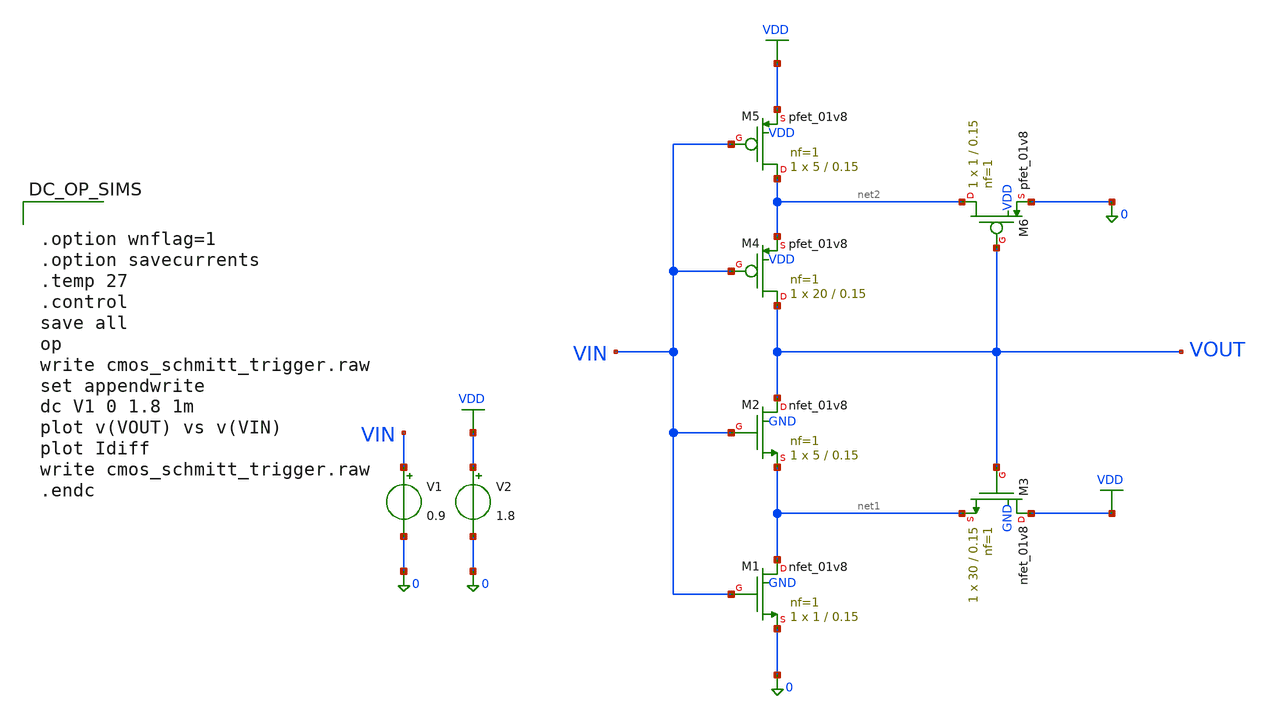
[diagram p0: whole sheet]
** sch_path: POR/cmos_sachmitt_trigger.sch
**.subckt cmos_sachmitt_trigger
XM1 net1 VIN 0 GND sky130_fd_pr__nfet_01v8 L=0.15 W=1 nf=1 ad='int((1 + 1)/2) * 1 / 1 * 0.29' as='int((1 + 2)/2) * 1 / 1 * 0.29'
+ pd='2*int((1 + 1)/2) * (1 / 1 + 0.29)' ps='2*int((1 + 2)/2) * (1 / 1 + 0.29)' nrd='0.29 / 1 ' nrs='0.29 / 1 '
+ sa=0 sb=0 sd=0 mult=1 m=1
XM2 VOUT VIN net1 GND sky130_fd_pr__nfet_01v8 L=0.15 W=5 nf=1 ad='int((1 + 1)/2) * 5 / 1 * 0.29' as='int((1 + 2)/2) * 5 / 1 * 0.29'
+ pd='2*int((1 + 1)/2) * (5 / 1 + 0.29)' ps='2*int((1 + 2)/2) * (5 / 1 + 0.29)' nrd='0.29 / 5 ' nrs='0.29 / 5 '
+ sa=0 sb=0 sd=0 mult=1 m=1
XM3 VDD VOUT net1 GND sky130_fd_pr__nfet_01v8 L=0.15 W=30 nf=1 ad='int((1 + 1)/2) * 30 / 1 * 0.29' as='int((1 + 2)/2) * 30 / 1 * 0.29'
+ pd='2*int((1 + 1)/2) * (30 / 1 + 0.29)' ps='2*int((1 + 2)/2) * (30 / 1 + 0.29)' nrd='0.29 / 30 ' nrs='0.29 / 30 '
+ sa=0 sb=0 sd=0 mult=1 m=1
XM4 VOUT VIN net2 VDD sky130_fd_pr__pfet_01v8 L=0.15 W=20 nf=1 ad='int((1 + 1)/2) * 20 / 1 * 0.29' as='int((1 + 2)/2) * 20 / 1 * 0.29'
+ pd='2*int((1 + 1)/2) * (20 / 1 + 0.29)' ps='2*int((1 + 2)/2) * (20 / 1 + 0.29)' nrd='0.29 / 20 ' nrs='0.29 / 20 '
+ sa=0 sb=0 sd=0 mult=1 m=1
XM5 net2 VIN VDD VDD sky130_fd_pr__pfet_01v8 L=0.15 W=5 nf=1 ad='int((1 + 1)/2) * 5 / 1 * 0.29' as='int((1 + 2)/2) * 5 / 1 * 0.29'
+ pd='2*int((1 + 1)/2) * (5 / 1 + 0.29)' ps='2*int((1 + 2)/2) * (5 / 1 + 0.29)' nrd='0.29 / 5 ' nrs='0.29 / 5 '
+ sa=0 sb=0 sd=0 mult=1 m=1
XM6 net2 VOUT 0 VDD sky130_fd_pr__pfet_01v8 L=0.15 W=1 nf=1 ad='int((1 + 1)/2) * 1 / 1 * 0.29' as='int((1 + 2)/2) * 1 / 1 * 0.29'
+ pd='2*int((1 + 1)/2) * (1 / 1 + 0.29)' ps='2*int((1 + 2)/2) * (1 / 1 + 0.29)' nrd='0.29 / 1 ' nrs='0.29 / 1 '
+ sa=0 sb=0 sd=0 mult=1 m=1
V2 VDD 0 1.8
V1 VIN 0 0.9
**** begin user architecture code


.option wnflag=1
.option savecurrents
.temp 27
.control
save all
op
write cmos_schmitt_trigger.raw
set appendwrite
dc V1 0 1.8 1m
plot v(VOUT) vs v(VIN)
plot Idiff
write cmos_schmitt_trigger.raw
.endc



** opencircuitdesign pdks install
.lib $::SKYWATER_MODELS/sky130.lib.spice tt

**** end user architecture code
**.ends
.GLOBAL VDD
.end
